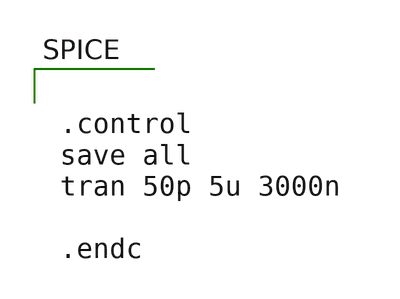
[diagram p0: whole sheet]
** sch_path: xschem/main.sch
**.subckt main
**** begin user architecture code

.include /foss/pdks/gf180mcuC/libs.tech/ngspice/design.ngspice
.lib /foss/pdks/gf180mcuC/libs.tech/ngspice/sm141064.ngspice typical
.lib /foss/pdks/gf180mcuC/libs.tech/ngspice/sm141064.ngspice mimcap_statistical
.lib /foss/pdks/gf180mcuC/libs.tech/ngspice/sm141064.ngspice cap_mim



.control
save all
tran 50p 5u 3000n

.endc

**** end user architecture code
**.ends
.end
